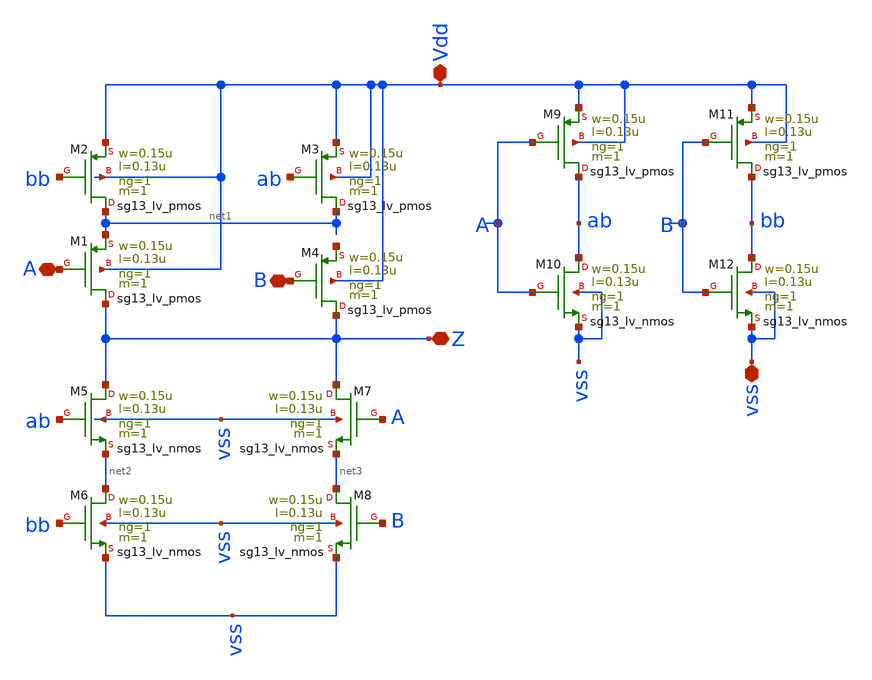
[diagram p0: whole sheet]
** sch_path: design/blocks/puertaxor/puertaxor.sch
**.subckt puertaxor A B vss Z Vdd
*.iopin A
*.iopin B
*.iopin vss
*.iopin Z
*.iopin Vdd
XM1 Z A net1 Vdd sg13_lv_pmos w=0.15u l=0.13u ng=1 m=1 mm_ok=1
XM2 net1 bb Vdd Vdd sg13_lv_pmos w=0.15u l=0.13u ng=1 m=1 mm_ok=1
XM3 net1 ab Vdd Vdd sg13_lv_pmos w=0.15u l=0.13u ng=1 m=1 mm_ok=1
XM4 Z B net4 Vdd sg13_lv_pmos w=0.15u l=0.13u ng=1 m=1 mm_ok=1
XM5 Z ab net2 vss sg13_lv_nmos w=0.15u l=0.13u ng=1 m=1 mm_ok=1
XM6 net2 bb vss vss sg13_lv_nmos w=0.15u l=0.13u ng=1 m=1 mm_ok=1
XM7 Z A net3 vss sg13_lv_nmos w=0.15u l=0.13u ng=1 m=1 mm_ok=1
XM8 net3 B vss vss sg13_lv_nmos w=0.15u l=0.13u ng=1 m=1 mm_ok=1
XM9 ab A Vdd Vdd sg13_lv_pmos w=0.15u l=0.13u ng=1 m=1 mm_ok=1
XM10 ab A vss vss sg13_lv_nmos w=0.15u l=0.13u ng=1 m=1 mm_ok=1
XM11 bb B Vdd Vdd sg13_lv_pmos w=0.15u l=0.13u ng=1 m=1 mm_ok=1
XM12 bb B vss vss sg13_lv_nmos w=0.15u l=0.13u ng=1 m=1 mm_ok=1
**.ends
.end
